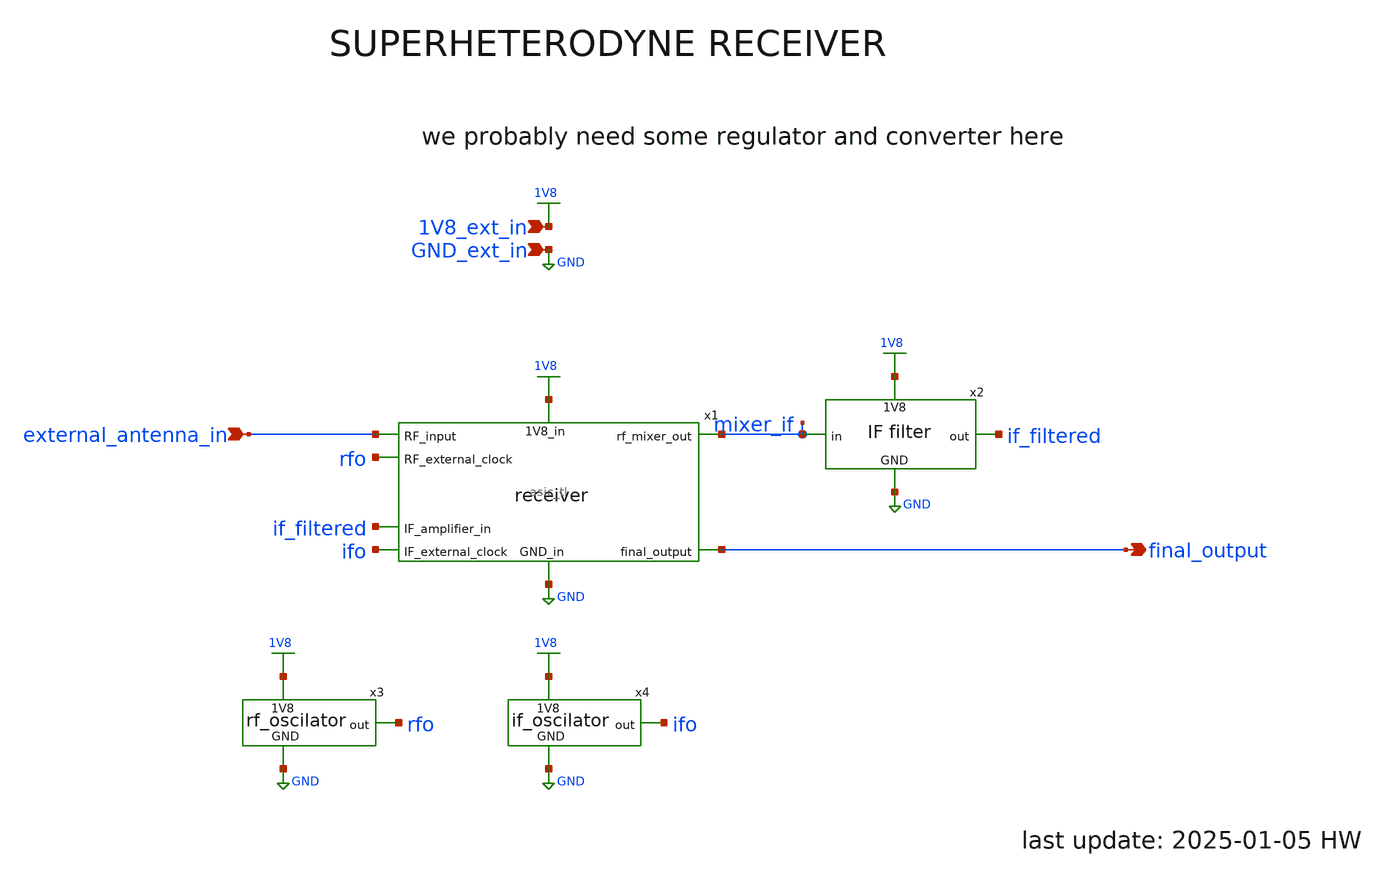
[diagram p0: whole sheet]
** sch_path: schematic/top_level.sch
**.subckt top_level 1V8_ext_in GND_ext_in external_antenna_in final_output
*.ipin 1V8_ext_in
*.ipin GND_ext_in
*.ipin external_antenna_in
*.opin final_output
x1 1V8 GND mixer_if external_antenna_in rfo final_output ifo if_filtered asic_tl
x2 1V8 mixer_if if_filtered GND if_filter
x3 1V8 rfo GND rf_oscilator
x4 1V8 ifo GND if_oscilator
**.ends
.GLOBAL 1V8
.GLOBAL GND
.end
